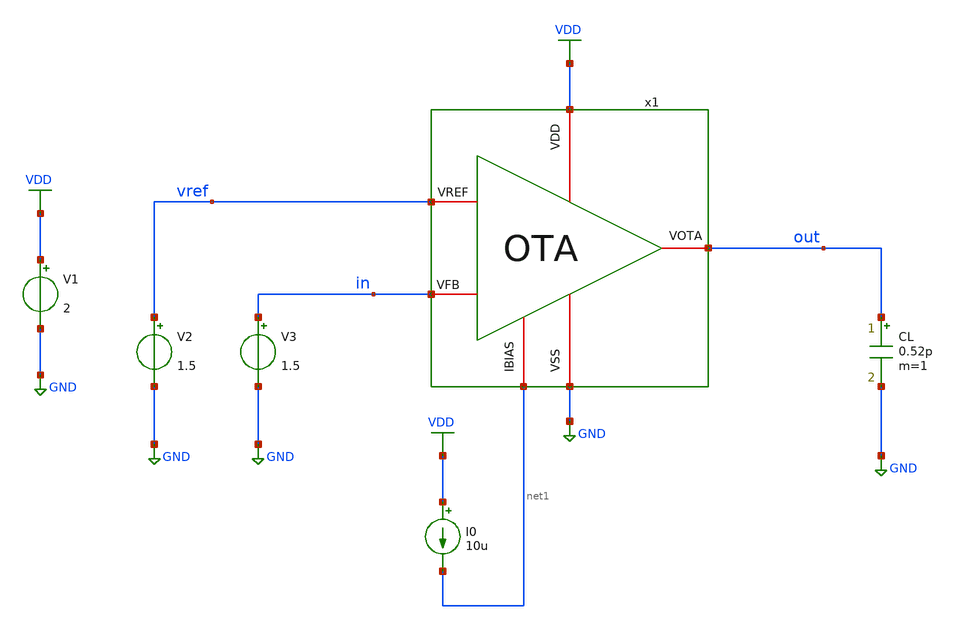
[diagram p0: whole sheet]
** sch_path: designs/libs/tb_ldo/tb_ldo/tb_ldo_OTA/tb_ldo_OTA_psrr/tb_ldo_OTA_psrr.sch
**.subckt tb_ldo_OTA_psrr
V1 VDD GND 2
V2 vref GND 1.5
I0 VDD net1 10u
CL out GND 0.52p m=1
V3 in GND 1.5
x1 VDD vref in out net1 GND OTA
**** begin user architecture code



.control
save all

** Set sources
alter @V1[AC] = 1

** Simulations
ac dec 100 1 10G

** Plots
setplot ac1
let psrr_db = db(v(out))
plot psrr_db

** Measurements
meas ac PSRR_gain FIND psrr_db AT=1Hz
let psrr_3db = PSRR_gain + 3
meas ac f_3db WHEN psrr_db=$&psrr_3db

write tb_ldo_OTA_psrr.raw

.endc
* ngspice commands




.include $::180MCU_MODELS/design.ngspice
.lib $::180MCU_MODELS/sm141064.ngspice typical
.lib $::180MCU_MODELS/sm141064.ngspice cap_mim
.lib $::180MCU_MODELS/sm141064.ngspice moscap_typical
.lib $::180MCU_MODELS/sm141064.ngspice mimcap_typical
.lib $::180MCU_MODELS/sm141064.ngspice res_typical
* .lib $::180MCU_MODELS/sm141064.ngspice res_statistical
* ngspice commands

**** end user architecture code
**.ends

* expanding   symbol:  libs/core_ldo/ldo/ldo_OTA/OTA.sym # of pins=6
** sym_path: designs/libs/core_ldo/ldo/OTA.sym
** sch_path: designs/libs/core_ldo/ldo/OTA.sch
.subckt OTA VDD VREF VFB VOTA IBIAS VSS
*.iopin VDD
*.iopin VSS
*.iopin VOTA
*.iopin VREF
*.iopin IBIAS
*.iopin VFB
XM3 net2 net2 VDD VDD pfet_05v0 L=2.00u W=8.00u nf=1 ad='int((nf+1)/2) * W/nf * 0.18u' as='int((nf+2)/2) * W/nf * 0.18u'
+ pd='2*int((nf+1)/2) * (W/nf + 0.18u)' ps='2*int((nf+2)/2) * (W/nf + 0.18u)' nrd='0.18u / W' nrs='0.18u / W'
+ sa=0 sb=0 sd=0 m=1
XM4 net3 net3 VDD VDD pfet_05v0 L=2.00u W=8.00u nf=1 ad='int((nf+1)/2) * W/nf * 0.18u' as='int((nf+2)/2) * W/nf * 0.18u'
+ pd='2*int((nf+1)/2) * (W/nf + 0.18u)' ps='2*int((nf+2)/2) * (W/nf + 0.18u)' nrd='0.18u / W' nrs='0.18u / W'
+ sa=0 sb=0 sd=0 m=1
XM5 net4 net2 VDD VDD pfet_05v0 L=2.00u W=8.00u nf=1 ad='int((nf+1)/2) * W/nf * 0.18u' as='int((nf+2)/2) * W/nf * 0.18u'
+ pd='2*int((nf+1)/2) * (W/nf + 0.18u)' ps='2*int((nf+2)/2) * (W/nf + 0.18u)' nrd='0.18u / W' nrs='0.18u / W'
+ sa=0 sb=0 sd=0 m=1
XM6 VOTA net3 VDD VDD pfet_05v0 L=2.00u W=8.00u nf=1 ad='int((nf+1)/2) * W/nf * 0.18u' as='int((nf+2)/2) * W/nf * 0.18u'
+ pd='2*int((nf+1)/2) * (W/nf + 0.18u)' ps='2*int((nf+2)/2) * (W/nf + 0.18u)' nrd='0.18u / W' nrs='0.18u / W'
+ sa=0 sb=0 sd=0 m=2
XM9 IBIAS IBIAS VSS VSS nfet_05v0 L=2.00u W=4.00u nf=1 ad='int((nf+1)/2) * W/nf * 0.18u' as='int((nf+2)/2) * W/nf * 0.18u'
+ pd='2*int((nf+1)/2) * (W/nf + 0.18u)' ps='2*int((nf+2)/2) * (W/nf + 0.18u)' nrd='0.18u / W' nrs='0.18u / W'
+ sa=0 sb=0 sd=0 m=1
XM10 net1 IBIAS VSS VSS nfet_05v0 L=2.00u W=4.00u nf=1 ad='int((nf+1)/2) * W/nf * 0.18u' as='int((nf+2)/2) * W/nf * 0.18u'
+ pd='2*int((nf+1)/2) * (W/nf + 0.18u)' ps='2*int((nf+2)/2) * (W/nf + 0.18u)' nrd='0.18u / W' nrs='0.18u / W'
+ sa=0 sb=0 sd=0 m=1
XM7 net4 net4 VSS VSS nfet_05v0 L=2.00u W=4.00u nf=1 ad='int((nf+1)/2) * W/nf * 0.18u' as='int((nf+2)/2) * W/nf * 0.18u'
+ pd='2*int((nf+1)/2) * (W/nf + 0.18u)' ps='2*int((nf+2)/2) * (W/nf + 0.18u)' nrd='0.18u / W' nrs='0.18u / W'
+ sa=0 sb=0 sd=0 m=1
XM8 VOTA net4 VSS VSS nfet_05v0 L=2.00u W=4.00u nf=1 ad='int((nf+1)/2) * W/nf * 0.18u' as='int((nf+2)/2) * W/nf * 0.18u'
+ pd='2*int((nf+1)/2) * (W/nf + 0.18u)' ps='2*int((nf+2)/2) * (W/nf + 0.18u)' nrd='0.18u / W' nrs='0.18u / W'
+ sa=0 sb=0 sd=0 m=2
XM1 net2 VREF net1 net1 nfet_05v0 L=0.60u W=40.00u nf=1 ad='int((nf+1)/2) * W/nf * 0.18u' as='int((nf+2)/2) * W/nf * 0.18u'
+ pd='2*int((nf+1)/2) * (W/nf + 0.18u)' ps='2*int((nf+2)/2) * (W/nf + 0.18u)' nrd='0.18u / W' nrs='0.18u / W'
+ sa=0 sb=0 sd=0 m=1
XM2 net3 VFB net1 net1 nfet_05v0 L=0.60u W=40.00u nf=1 ad='int((nf+1)/2) * W/nf * 0.18u' as='int((nf+2)/2) * W/nf * 0.18u'
+ pd='2*int((nf+1)/2) * (W/nf + 0.18u)' ps='2*int((nf+2)/2) * (W/nf + 0.18u)' nrd='0.18u / W' nrs='0.18u / W'
+ sa=0 sb=0 sd=0 m=1
.ends

.GLOBAL GND
.GLOBAL VDD
.end
